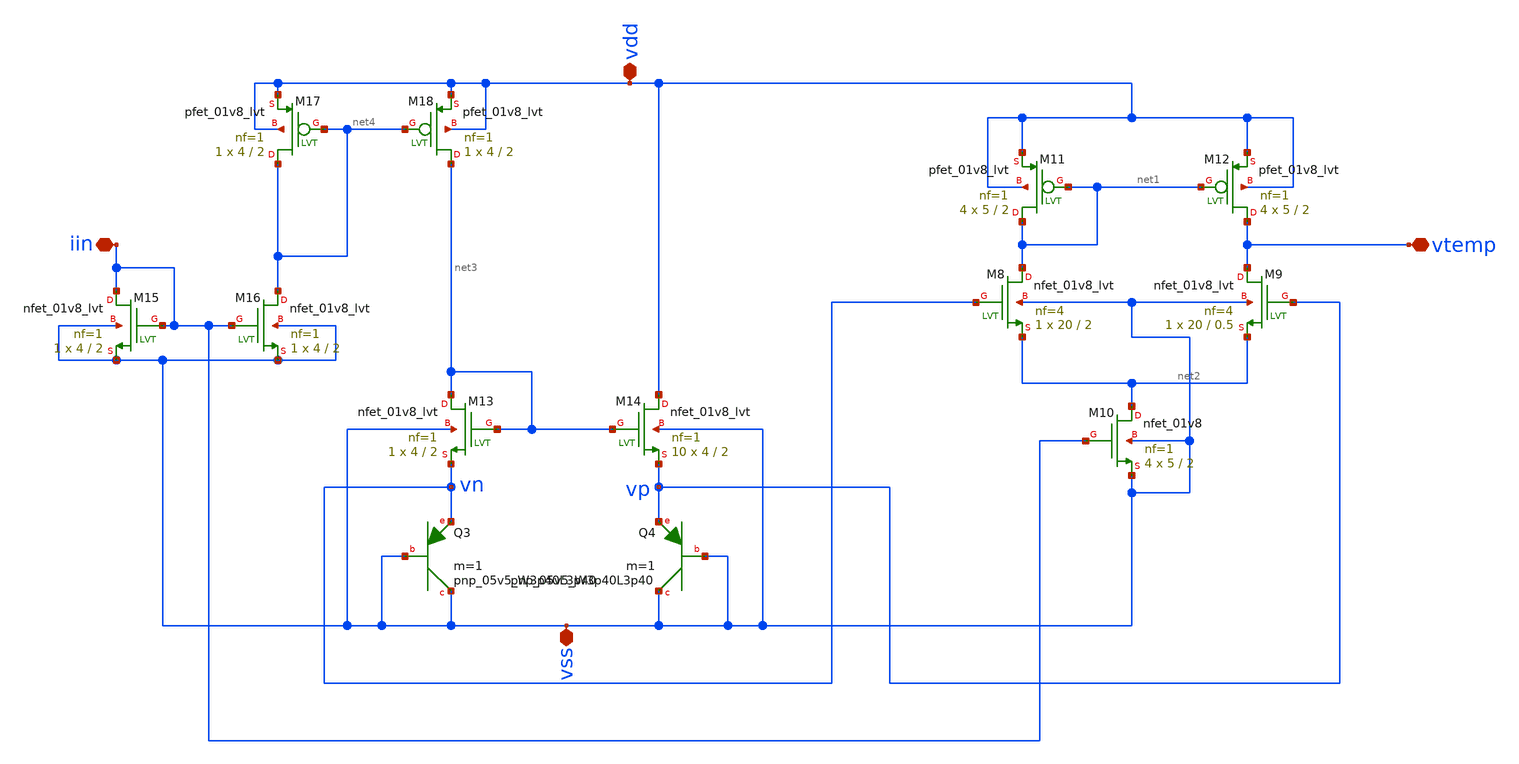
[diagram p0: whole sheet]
** sch_path: ANOTHER_SOLUTIONS_CONSIDERED/ANOTHER_BIAS_FOR_TEMPERATURE_SENSOR/TEMPERATURE_SENSOR/XSCHEM/Temperature_Sensor.sch
**.subckt Temperature_Sensor vdd vss vtemp iin
*.iopin vdd
*.iopin vss
*.iopin vtemp
*.iopin iin
XM8 net1 vn net2 vss sky130_fd_pr__nfet_01v8_lvt L=2 W=20 nf=4 ad='int((nf+1)/2) * W/nf * 0.29' as='int((nf+2)/2) * W/nf * 0.29'
+ pd='2*int((nf+1)/2) * (W/nf + 0.29)' ps='2*int((nf+2)/2) * (W/nf + 0.29)' nrd='0.29 / W' nrs='0.29 / W'
+ sa=0 sb=0 sd=0 mult=1 m=1
XM9 vtemp vp net2 vss sky130_fd_pr__nfet_01v8_lvt L=0.5 W=20 nf=4 ad='int((nf+1)/2) * W/nf * 0.29' as='int((nf+2)/2) * W/nf * 0.29'
+ pd='2*int((nf+1)/2) * (W/nf + 0.29)' ps='2*int((nf+2)/2) * (W/nf + 0.29)' nrd='0.29 / W' nrs='0.29 / W'
+ sa=0 sb=0 sd=0 mult=1 m=1
XM10 net2 iin vss vss sky130_fd_pr__nfet_01v8 L=2 W=5 nf=1 ad='int((nf+1)/2) * W/nf * 0.29' as='int((nf+2)/2) * W/nf * 0.29'
+ pd='2*int((nf+1)/2) * (W/nf + 0.29)' ps='2*int((nf+2)/2) * (W/nf + 0.29)' nrd='0.29 / W' nrs='0.29 / W'
+ sa=0 sb=0 sd=0 mult=4 m=4
XM11 net1 net1 vdd vdd sky130_fd_pr__pfet_01v8_lvt L=2 W=5 nf=1 ad='int((nf+1)/2) * W/nf * 0.29' as='int((nf+2)/2) * W/nf * 0.29'
+ pd='2*int((nf+1)/2) * (W/nf + 0.29)' ps='2*int((nf+2)/2) * (W/nf + 0.29)' nrd='0.29 / W' nrs='0.29 / W'
+ sa=0 sb=0 sd=0 mult=4 m=4
XM12 vtemp net1 vdd vdd sky130_fd_pr__pfet_01v8_lvt L=2 W=5 nf=1 ad='int((nf+1)/2) * W/nf * 0.29' as='int((nf+2)/2) * W/nf * 0.29'
+ pd='2*int((nf+1)/2) * (W/nf + 0.29)' ps='2*int((nf+2)/2) * (W/nf + 0.29)' nrd='0.29 / W' nrs='0.29 / W'
+ sa=0 sb=0 sd=0 mult=4 m=4
XM13 net3 net3 vn vss sky130_fd_pr__nfet_01v8_lvt L=2 W=4 nf=1 ad='int((nf+1)/2) * W/nf * 0.29' as='int((nf+2)/2) * W/nf * 0.29'
+ pd='2*int((nf+1)/2) * (W/nf + 0.29)' ps='2*int((nf+2)/2) * (W/nf + 0.29)' nrd='0.29 / W' nrs='0.29 / W'
+ sa=0 sb=0 sd=0 mult=1 m=1
XQ3 vss vss vn sky130_fd_pr__pnp_05v5_W3p40L3p40 m=1
XM14 vdd net3 vp vss sky130_fd_pr__nfet_01v8_lvt L=2 W=4 nf=1 ad='int((nf+1)/2) * W/nf * 0.29' as='int((nf+2)/2) * W/nf * 0.29'
+ pd='2*int((nf+1)/2) * (W/nf + 0.29)' ps='2*int((nf+2)/2) * (W/nf + 0.29)' nrd='0.29 / W' nrs='0.29 / W'
+ sa=0 sb=0 sd=0 mult=10 m=10
XQ4 vss vss vp sky130_fd_pr__pnp_05v5_W3p40L3p40 m=1
XM15 iin iin vss vss sky130_fd_pr__nfet_01v8_lvt L=2 W=4 nf=1 ad='int((nf+1)/2) * W/nf * 0.29' as='int((nf+2)/2) * W/nf * 0.29'
+ pd='2*int((nf+1)/2) * (W/nf + 0.29)' ps='2*int((nf+2)/2) * (W/nf + 0.29)' nrd='0.29 / W' nrs='0.29 / W'
+ sa=0 sb=0 sd=0 mult=1 m=1
XM16 net4 iin vss vss sky130_fd_pr__nfet_01v8_lvt L=2 W=4 nf=1 ad='int((nf+1)/2) * W/nf * 0.29' as='int((nf+2)/2) * W/nf * 0.29'
+ pd='2*int((nf+1)/2) * (W/nf + 0.29)' ps='2*int((nf+2)/2) * (W/nf + 0.29)' nrd='0.29 / W' nrs='0.29 / W'
+ sa=0 sb=0 sd=0 mult=1 m=1
XM17 net4 net4 vdd vdd sky130_fd_pr__pfet_01v8_lvt L=2 W=4 nf=1 ad='int((nf+1)/2) * W/nf * 0.29' as='int((nf+2)/2) * W/nf * 0.29'
+ pd='2*int((nf+1)/2) * (W/nf + 0.29)' ps='2*int((nf+2)/2) * (W/nf + 0.29)' nrd='0.29 / W' nrs='0.29 / W'
+ sa=0 sb=0 sd=0 mult=1 m=1
XM18 net3 net4 vdd vdd sky130_fd_pr__pfet_01v8_lvt L=2 W=4 nf=1 ad='int((nf+1)/2) * W/nf * 0.29' as='int((nf+2)/2) * W/nf * 0.29'
+ pd='2*int((nf+1)/2) * (W/nf + 0.29)' ps='2*int((nf+2)/2) * (W/nf + 0.29)' nrd='0.29 / W' nrs='0.29 / W'
+ sa=0 sb=0 sd=0 mult=1 m=1
**.ends
.end
